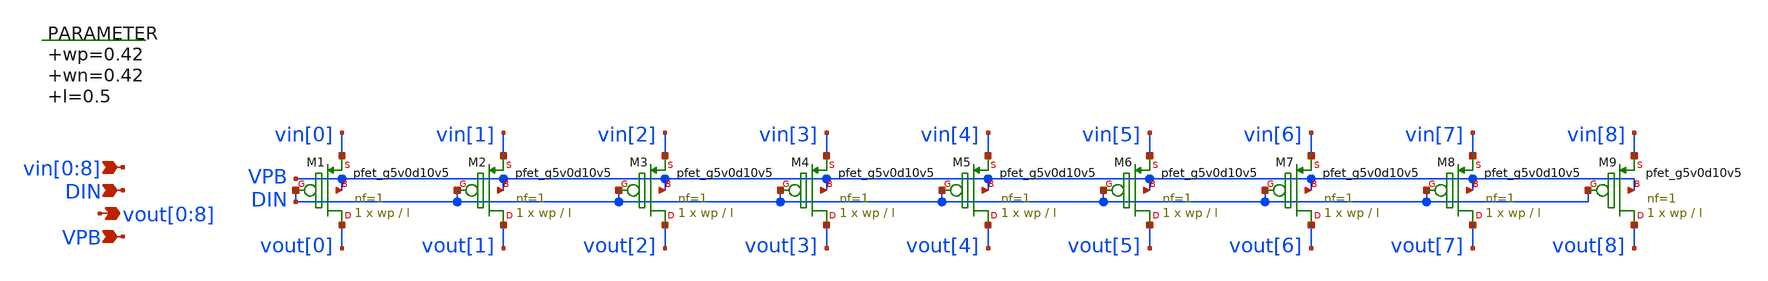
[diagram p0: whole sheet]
** sch_path: xschem/switch_pmos_1g_9o.sch
**.subckt switch_pmos_1g_9o vin[0],vin[1],vin[2],vin[3],vin[4],vin[5],vin[6],vin[7],vin[8]
*+ vout[0],vout[1],vout[2],vout[3],vout[4],vout[5],vout[6],vout[7],vout[8] VPB DIN
*.ipin vin[0],vin[1],vin[2],vin[3],vin[4],vin[5],vin[6],vin[7],vin[8]
*.opin vout[0],vout[1],vout[2],vout[3],vout[4],vout[5],vout[6],vout[7],vout[8]
*.ipin VPB
*.ipin DIN
.param wp=0.42 wn=0.42 l=0.5

XM1 vout[0] DIN vin[0] VPB sky130_fd_pr__pfet_g5v0d10v5 L=l W=wp nf=1 ad='int((nf+1)/2) * W/nf * 0.29'
+ as='int((nf+2)/2) * W/nf * 0.29' pd='2*int((nf+1)/2) * (W/nf + 0.29)' ps='2*int((nf+2)/2) * (W/nf + 0.29)'
+ nrd='0.29 / W' nrs='0.29 / W' sa=0 sb=0 sd=0 mult=1 m=1
XM2 vout[1] DIN vin[1] VPB sky130_fd_pr__pfet_g5v0d10v5 L=l W=wp nf=1 ad='int((nf+1)/2) * W/nf * 0.29'
+ as='int((nf+2)/2) * W/nf * 0.29' pd='2*int((nf+1)/2) * (W/nf + 0.29)' ps='2*int((nf+2)/2) * (W/nf + 0.29)'
+ nrd='0.29 / W' nrs='0.29 / W' sa=0 sb=0 sd=0 mult=1 m=1
XM3 vout[2] DIN vin[2] VPB sky130_fd_pr__pfet_g5v0d10v5 L=l W=wp nf=1 ad='int((nf+1)/2) * W/nf * 0.29'
+ as='int((nf+2)/2) * W/nf * 0.29' pd='2*int((nf+1)/2) * (W/nf + 0.29)' ps='2*int((nf+2)/2) * (W/nf + 0.29)'
+ nrd='0.29 / W' nrs='0.29 / W' sa=0 sb=0 sd=0 mult=1 m=1
XM4 vout[3] DIN vin[3] VPB sky130_fd_pr__pfet_g5v0d10v5 L=l W=wp nf=1 ad='int((nf+1)/2) * W/nf * 0.29'
+ as='int((nf+2)/2) * W/nf * 0.29' pd='2*int((nf+1)/2) * (W/nf + 0.29)' ps='2*int((nf+2)/2) * (W/nf + 0.29)'
+ nrd='0.29 / W' nrs='0.29 / W' sa=0 sb=0 sd=0 mult=1 m=1
XM5 vout[4] DIN vin[4] VPB sky130_fd_pr__pfet_g5v0d10v5 L=l W=wp nf=1 ad='int((nf+1)/2) * W/nf * 0.29'
+ as='int((nf+2)/2) * W/nf * 0.29' pd='2*int((nf+1)/2) * (W/nf + 0.29)' ps='2*int((nf+2)/2) * (W/nf + 0.29)'
+ nrd='0.29 / W' nrs='0.29 / W' sa=0 sb=0 sd=0 mult=1 m=1
XM6 vout[5] DIN vin[5] VPB sky130_fd_pr__pfet_g5v0d10v5 L=l W=wp nf=1 ad='int((nf+1)/2) * W/nf * 0.29'
+ as='int((nf+2)/2) * W/nf * 0.29' pd='2*int((nf+1)/2) * (W/nf + 0.29)' ps='2*int((nf+2)/2) * (W/nf + 0.29)'
+ nrd='0.29 / W' nrs='0.29 / W' sa=0 sb=0 sd=0 mult=1 m=1
XM7 vout[6] DIN vin[6] VPB sky130_fd_pr__pfet_g5v0d10v5 L=l W=wp nf=1 ad='int((nf+1)/2) * W/nf * 0.29'
+ as='int((nf+2)/2) * W/nf * 0.29' pd='2*int((nf+1)/2) * (W/nf + 0.29)' ps='2*int((nf+2)/2) * (W/nf + 0.29)'
+ nrd='0.29 / W' nrs='0.29 / W' sa=0 sb=0 sd=0 mult=1 m=1
XM8 vout[7] DIN vin[7] VPB sky130_fd_pr__pfet_g5v0d10v5 L=l W=wp nf=1 ad='int((nf+1)/2) * W/nf * 0.29'
+ as='int((nf+2)/2) * W/nf * 0.29' pd='2*int((nf+1)/2) * (W/nf + 0.29)' ps='2*int((nf+2)/2) * (W/nf + 0.29)'
+ nrd='0.29 / W' nrs='0.29 / W' sa=0 sb=0 sd=0 mult=1 m=1
XM9 vout[8] DIN vin[8] VPB sky130_fd_pr__pfet_g5v0d10v5 L=l W=wp nf=1 ad='int((nf+1)/2) * W/nf * 0.29'
+ as='int((nf+2)/2) * W/nf * 0.29' pd='2*int((nf+1)/2) * (W/nf + 0.29)' ps='2*int((nf+2)/2) * (W/nf + 0.29)'
+ nrd='0.29 / W' nrs='0.29 / W' sa=0 sb=0 sd=0 mult=1 m=1
**.ends
.end
